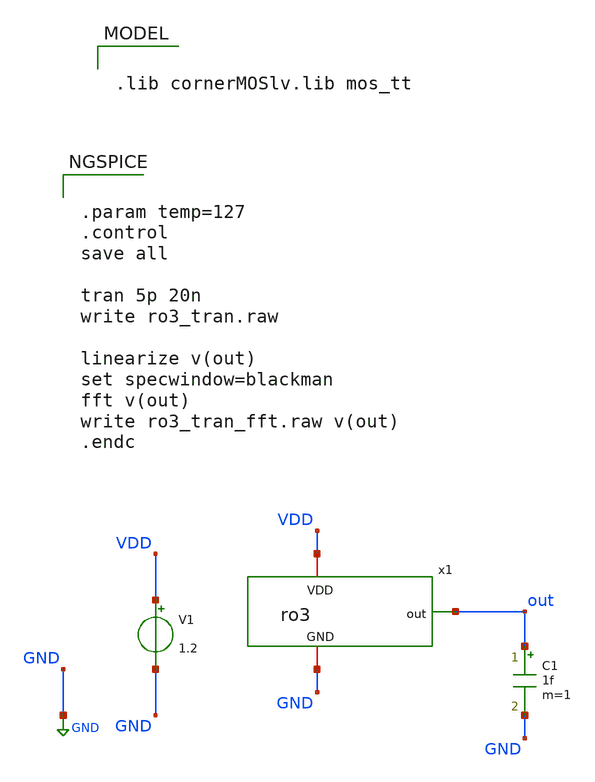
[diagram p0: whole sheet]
** sch_path: 20260718_ring_oscillator/ro3_tb.sch
**.subckt ro3_tb
x1 out VDD GND ro3
V1 VDD GND 1.2
C1 out GND 1f m=1
**** begin user architecture code

.lib cornerMOSlv.lib mos_tt



.param temp=127
.control
save all

tran 5p 20n
write ro3_tran.raw

linearize v(out)
set specwindow=blackman
fft v(out)
write ro3_tran_fft.raw v(out)
.endc


**** end user architecture code
**.ends

* expanding   symbol:  ro3.sym # of pins=3
** sym_path: 20260719_tunnable_ring_oscillator/ro3.sym
** sch_path: 20260719_tunnable_ring_oscillator/ro3.sch
.subckt ro3 out VDD GND
*.opin out
*.iopin VDD
*.iopin GND
XM1 net1 net2 GND GND sg13_lv_nmos w=0.15u l=0.13u ng=1 m=1 mm_ok=1
XM2 net1 net2 VDD VDD sg13_lv_pmos w=0.3u l=0.13u ng=1 m=1 mm_ok=1
XM3 net3 net1 GND GND sg13_lv_nmos w=0.15u l=0.13u ng=1 m=1 mm_ok=1
XM4 net3 net1 VDD VDD sg13_lv_pmos w=0.3u l=0.13u ng=1 m=1 mm_ok=1
XM5 net2 net3 GND GND sg13_lv_nmos w=0.15u l=0.13u ng=1 m=1 mm_ok=1
XM6 net2 net3 VDD VDD sg13_lv_pmos w=0.3u l=0.13u ng=1 m=1 mm_ok=1
XM7 out net2 GND GND sg13_lv_nmos w=0.15u l=0.13u ng=1 m=1 mm_ok=1
XM8 out net2 VDD VDD sg13_lv_pmos w=0.3u l=0.13u ng=1 m=1 mm_ok=1
.ends

.GLOBAL GND
.end
